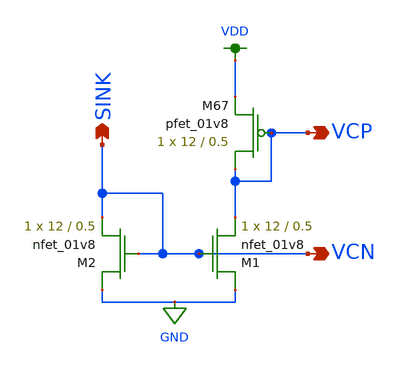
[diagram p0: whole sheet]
** sch_path: schemas/BIAS_VC.sch
**.subckt BIAS_VC VCN VCP SINK
*.opin VCN
*.opin VCP
*.opin SINK
XM67 VCP VCP VDD VDD sky130_fd_pr__pfet_01v8 L=0.5 W=12 nf=1 ad='int((nf+1)/2) * W/nf * 0.29' as='int((nf+2)/2) * W/nf * 0.29'
+ pd='2*int((nf+1)/2) * (W/nf + 0.29)' ps='2*int((nf+2)/2) * (W/nf + 0.29)' nrd='0.29 / W' nrs='0.29 / W'
+ sa=0 sb=0 sd=0 mult=1 m=1
XM2 GND VCN VCN GND sky130_fd_pr__nfet_01v8 L=0.5 W=12 nf=1 ad='int((nf+1)/2) * W/nf * 0.29' as='int((nf+2)/2) * W/nf * 0.29'
+ pd='2*int((nf+1)/2) * (W/nf + 0.29)' ps='2*int((nf+2)/2) * (W/nf + 0.29)' nrd='0.29 / W' nrs='0.29 / W'
+ sa=0 sb=0 sd=0 mult=1 m=1
XM1 GND VCN VCP GND sky130_fd_pr__nfet_01v8 L=0.5 W=12 nf=1 ad='int((nf+1)/2) * W/nf * 0.29' as='int((nf+2)/2) * W/nf * 0.29'
+ pd='2*int((nf+1)/2) * (W/nf + 0.29)' ps='2*int((nf+2)/2) * (W/nf + 0.29)' nrd='0.29 / W' nrs='0.29 / W'
+ sa=0 sb=0 sd=0 mult=1 m=1
**.ends
.GLOBAL VDD
.GLOBAL GND
.end
